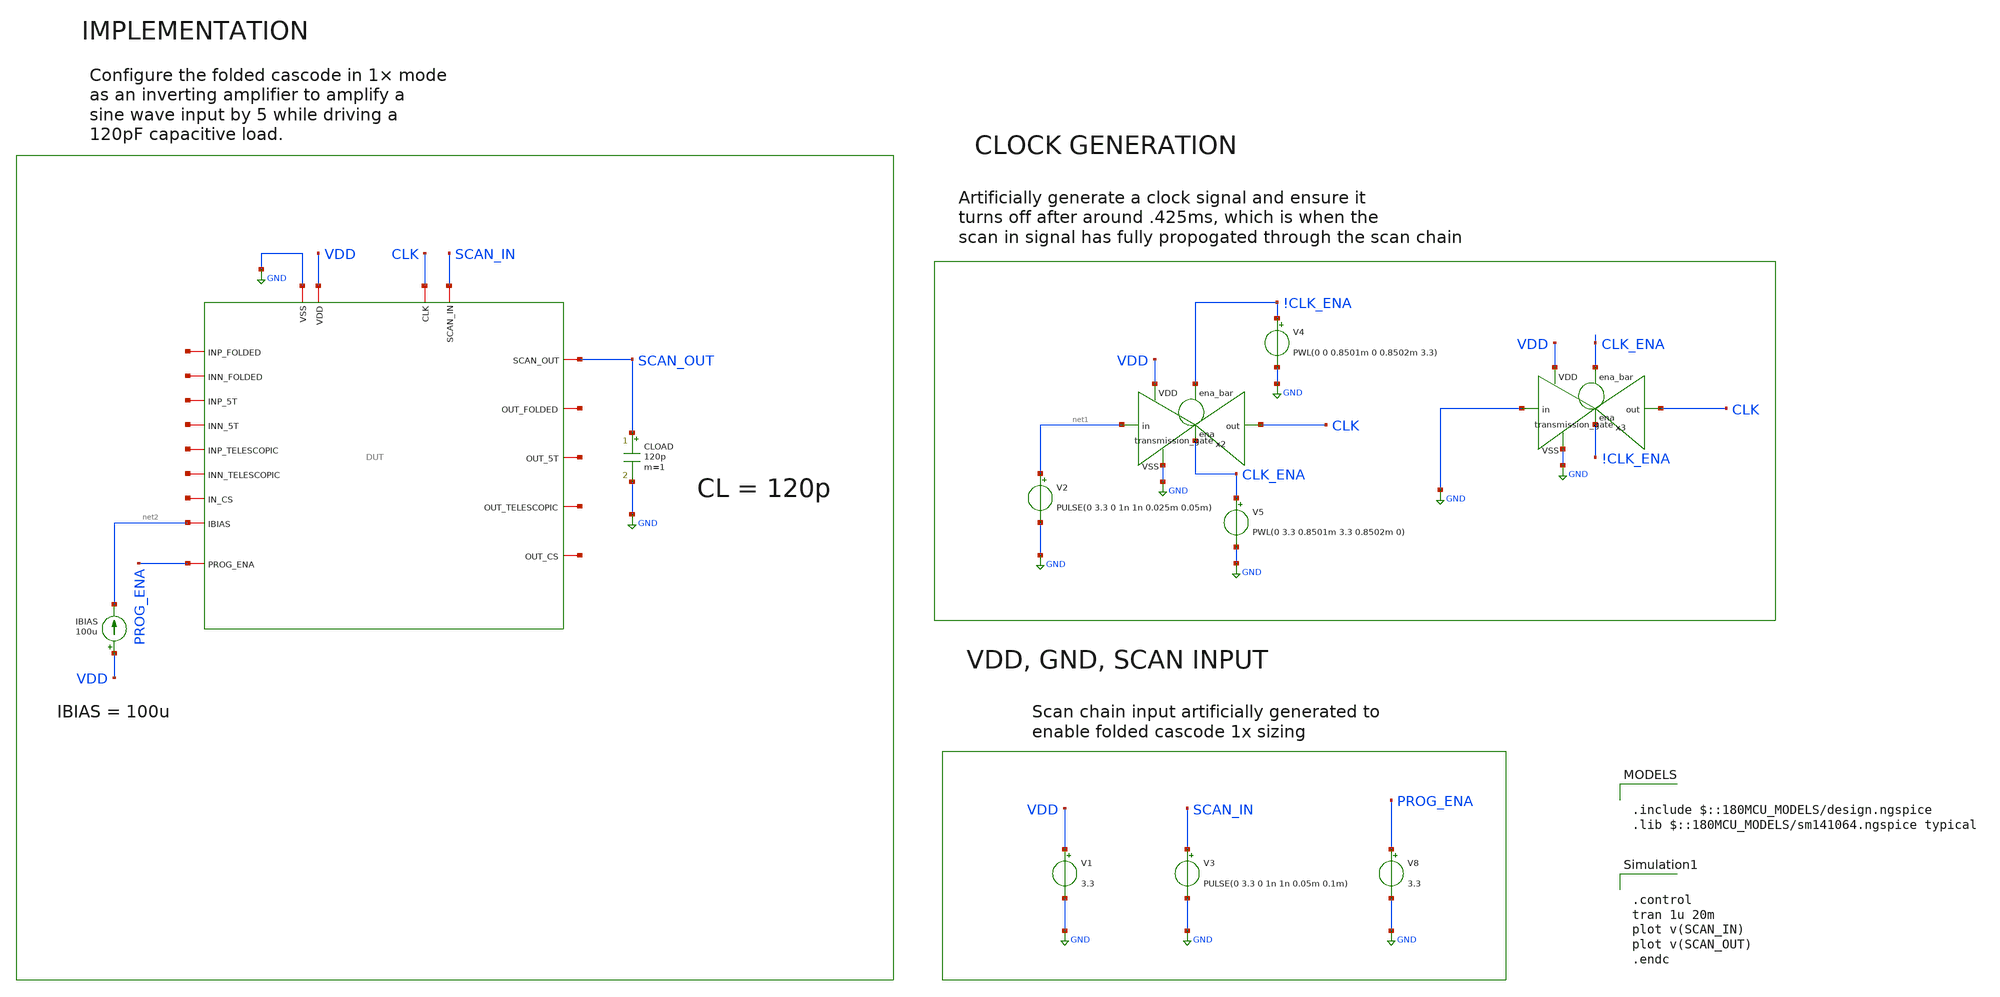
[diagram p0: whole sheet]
** sch_path: designs/libs/core_tb/mrd/tb_scan_out.sch
**.subckt tb_scan_out
V3 SCAN_IN GND PULSE(0 3.3 0 1n 1n 0.05m 0.1m)
V1 VDD GND 3.3
V2 net1 GND PULSE(0 3.3 0 1n 1n 0.025m 0.05m)
x2 !CLK_ENA VDD CLK net1 GND CLK_ENA transmission_gate
V4 !CLK_ENA GND PWL(0 0 0.8501m 0 0.8502m 3.3)
V5 CLK_ENA GND PWL(0 3.3 0.8501m 3.3 0.8502m 0)
IBIAS VDD net2 100u
CLOAD SCAN_OUT GND 120p m=1
x1 CLK SCAN_OUT SCAN_IN GND VDD net3 net4 net5 net2 net6 net7 net8 net9 net10 net11 net12 net13
+ PROG_ENA DUT
x3 CLK_ENA VDD CLK GND GND !CLK_ENA transmission_gate
V8 PROG_ENA GND 3.3
**** begin user architecture code

.include $::180MCU_MODELS/design.ngspice
.lib $::180MCU_MODELS/sm141064.ngspice typical



.control
tran 1u 20m
plot v(SCAN_IN)
plot v(SCAN_OUT)
.endc


**** end user architecture code
**.ends
.GLOBAL GND
.end
